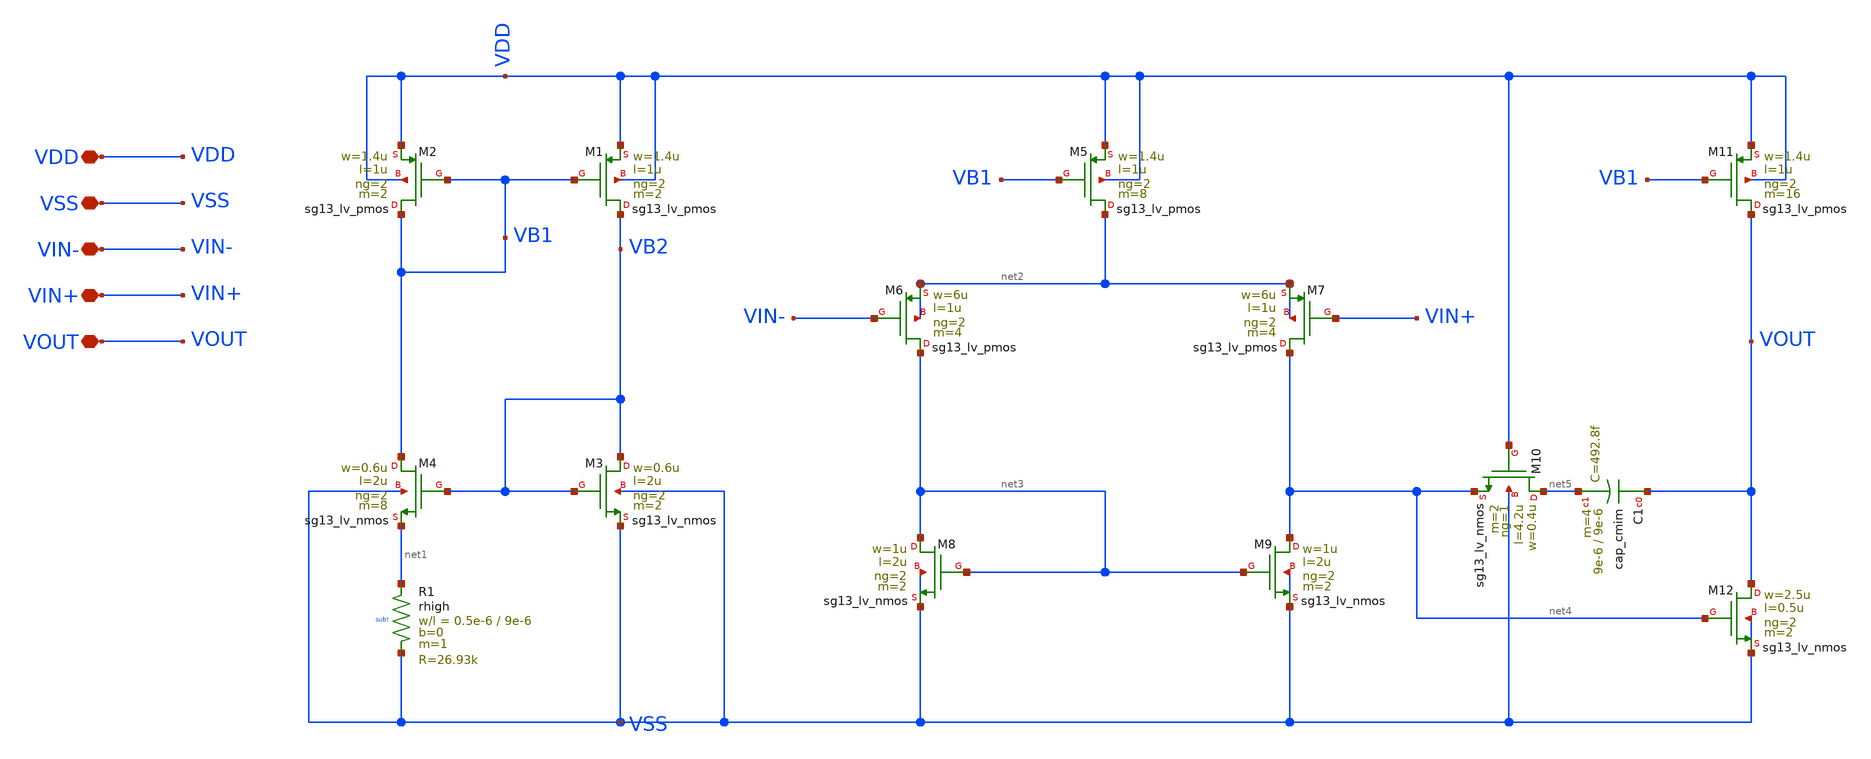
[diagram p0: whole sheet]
** sch_path: LIB/ihp-sg13g2/Amplifiers/Va001_ihp-sg13g2_1_2.sch
**.subckt Va001_ihp-sg13g2_1_2 VDD VSS VIN- VIN+ VOUT
*.iopin VDD
*.iopin VSS
*.iopin VIN-
*.iopin VIN+
*.iopin VOUT
XR1 net1 VSS sub! rhigh w=0.5e-6 l=9e-6 m=1 b=0 mm_ok=1
XM2 VB1 VB1 VDD VDD sg13_lv_pmos w=1.4u l=1u ng=2 m=2 mm_ok=1
XM1 VB2 VB1 VDD VDD sg13_lv_pmos w=1.4u l=1u ng=2 m=2 mm_ok=1
XM4 VB1 VB2 net1 VSS sg13_lv_nmos w=0.6u l=2u ng=2 m=8 mm_ok=1
XM3 VB2 VB2 VSS VSS sg13_lv_nmos w=0.6u l=2u ng=2 m=2 mm_ok=1
XM5 net2 VB1 VDD VDD sg13_lv_pmos w=1.4u l=1u ng=2 m=8 mm_ok=1
XM6 net3 VIN- net2 net2 sg13_lv_pmos w=6u l=1u ng=2 m=4 mm_ok=1
XM7 net4 VIN+ net2 net2 sg13_lv_pmos w=6u l=1u ng=2 m=4 mm_ok=1
XM8 net3 net3 VSS VSS sg13_lv_nmos w=1u l=2u ng=2 m=2 mm_ok=1
XM9 net4 net3 VSS VSS sg13_lv_nmos w=1u l=2u ng=2 m=2 mm_ok=1
XM10 net5 VDD net4 VSS sg13_lv_nmos w=0.4u l=4.2u ng=1 m=2 mm_ok=1
XC1 VOUT net5 cap_cmim w=9e-6 l=9e-6 m=4 mm_ok=1
XM11 VOUT VB1 VDD VDD sg13_lv_pmos w=1.4u l=1u ng=2 m=16 mm_ok=1
XM12 VOUT net4 VSS VSS sg13_lv_nmos w=2.5u l=0.5u ng=2 m=2 mm_ok=1
**.ends
.end
